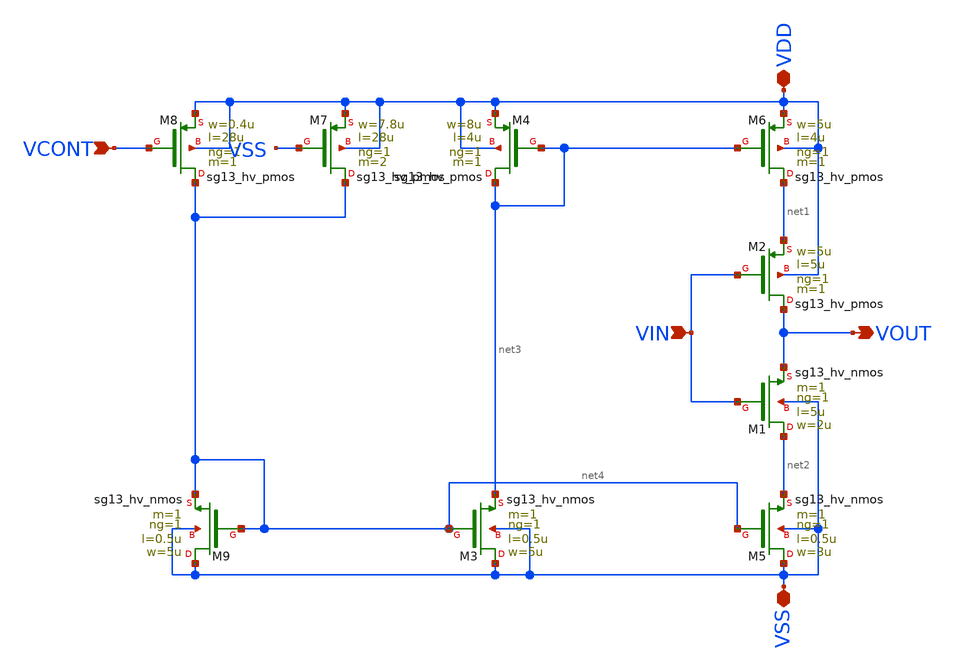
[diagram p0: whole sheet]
** sch_path: xschem/stage_v6p4_IHP.sch
**.subckt stage_v6p4_IHP VIN VOUT VDD VSS VCONT
*.ipin VIN
*.opin VOUT
*.iopin VDD
*.iopin VSS
*.ipin VCONT
XM9 VSS net4 net4 VSS sg13_hv_nmos w=5u l=0.5u ng=1 m=1 mm_ok=1
XM3 VSS net4 net3 VSS sg13_hv_nmos w=5u l=0.5u ng=1 m=1 mm_ok=1
XM5 VSS net4 net2 VSS sg13_hv_nmos w=3u l=0.5u ng=1 m=1 mm_ok=1
XM8 net4 VCONT VDD VDD sg13_hv_pmos w=0.4u l=28u ng=1 m=1 mm_ok=1
XM4 net3 net3 VDD VDD sg13_hv_pmos w=8u l=4u ng=1 m=1 mm_ok=1
XM6 net1 net3 VDD VDD sg13_hv_pmos w=5u l=4u ng=1 m=1 mm_ok=1
XM2 VOUT VIN net1 VDD sg13_hv_pmos w=5u l=5u ng=1 m=1 mm_ok=1
XM1 net2 VIN VOUT VSS sg13_hv_nmos w=2u l=5u ng=1 m=1 mm_ok=1
XM7 net4 VSS VDD VDD sg13_hv_pmos w=7.8u l=28u ng=1 m=2 mm_ok=1
**.ends
.end
